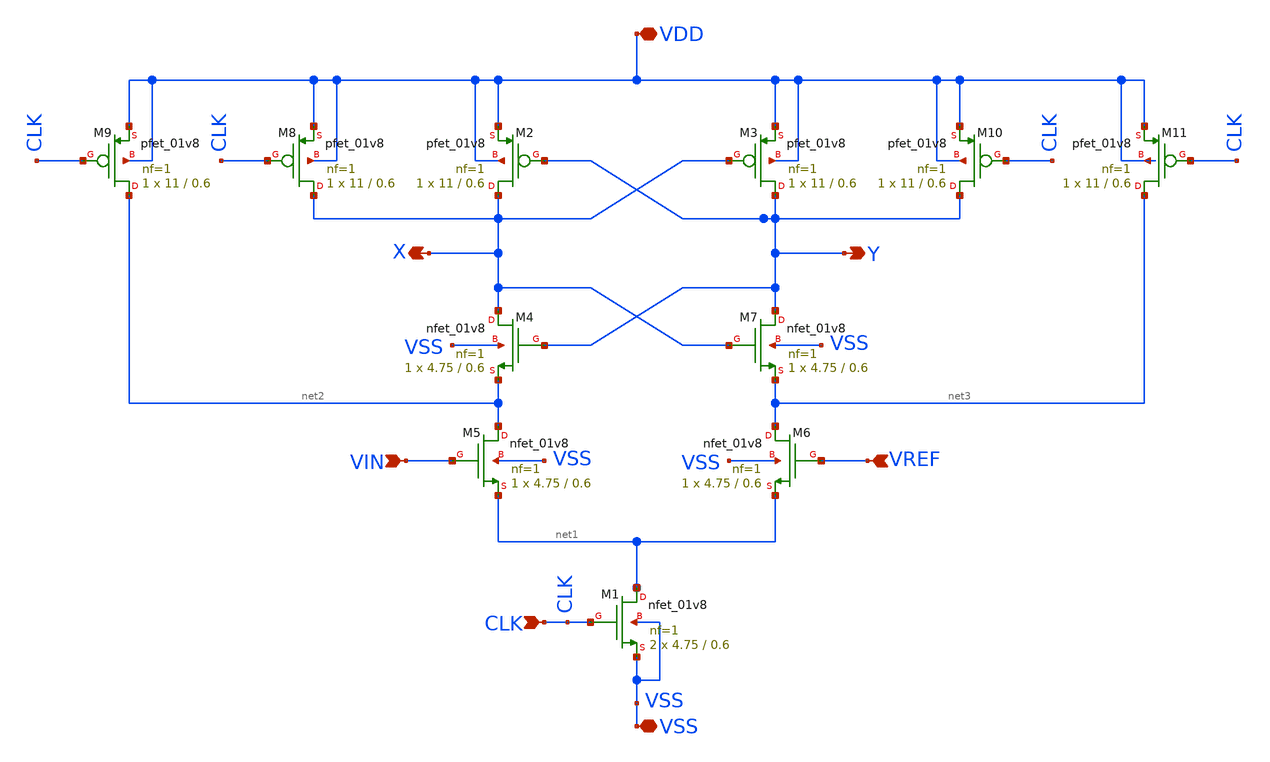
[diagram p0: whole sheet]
** sch_path: strongARM/strongARM_v1_sym.sch
**.subckt strongARM_v1_sym VDD VIN VREF Y X VSS CLK
*.iopin VDD
*.ipin VIN
*.ipin VREF
*.opin Y
*.opin X
*.iopin VSS
*.ipin CLK
XM1 net1 CLK VSS VSS sky130_fd_pr__nfet_01v8 L=0.6 W=4.75 nf=1 ad='int((nf+1)/2) * W/nf * 0.29' as='int((nf+2)/2) * W/nf * 0.29'
+ pd='2*int((nf+1)/2) * (W/nf + 0.29)' ps='2*int((nf+2)/2) * (W/nf + 0.29)' nrd='0.29 / W' nrs='0.29 / W'
+ sa=0 sb=0 sd=0 mult=2 m=2
XM2 X Y VDD VDD sky130_fd_pr__pfet_01v8 L=0.6 W=11 nf=1 ad='int((nf+1)/2) * W/nf * 0.29' as='int((nf+2)/2) * W/nf * 0.29'
+ pd='2*int((nf+1)/2) * (W/nf + 0.29)' ps='2*int((nf+2)/2) * (W/nf + 0.29)' nrd='0.29 / W' nrs='0.29 / W'
+ sa=0 sb=0 sd=0 mult=1 m=1
XM3 Y X VDD VDD sky130_fd_pr__pfet_01v8 L=0.6 W=11 nf=1 ad='int((nf+1)/2) * W/nf * 0.29' as='int((nf+2)/2) * W/nf * 0.29'
+ pd='2*int((nf+1)/2) * (W/nf + 0.29)' ps='2*int((nf+2)/2) * (W/nf + 0.29)' nrd='0.29 / W' nrs='0.29 / W'
+ sa=0 sb=0 sd=0 mult=1 m=1
XM5 net2 VIN net1 VSS sky130_fd_pr__nfet_01v8 L=0.6 W=4.75 nf=1 ad='int((nf+1)/2) * W/nf * 0.29' as='int((nf+2)/2) * W/nf * 0.29'
+ pd='2*int((nf+1)/2) * (W/nf + 0.29)' ps='2*int((nf+2)/2) * (W/nf + 0.29)' nrd='0.29 / W' nrs='0.29 / W'
+ sa=0 sb=0 sd=0 mult=1 m=1
XM4 X Y net2 VSS sky130_fd_pr__nfet_01v8 L=0.6 W=4.75 nf=1 ad='int((nf+1)/2) * W/nf * 0.29' as='int((nf+2)/2) * W/nf * 0.29'
+ pd='2*int((nf+1)/2) * (W/nf + 0.29)' ps='2*int((nf+2)/2) * (W/nf + 0.29)' nrd='0.29 / W' nrs='0.29 / W'
+ sa=0 sb=0 sd=0 mult=1 m=1
XM6 net3 VREF net1 VSS sky130_fd_pr__nfet_01v8 L=0.6 W=4.75 nf=1 ad='int((nf+1)/2) * W/nf * 0.29' as='int((nf+2)/2) * W/nf * 0.29'
+ pd='2*int((nf+1)/2) * (W/nf + 0.29)' ps='2*int((nf+2)/2) * (W/nf + 0.29)' nrd='0.29 / W' nrs='0.29 / W'
+ sa=0 sb=0 sd=0 mult=1 m=1
XM7 Y X net3 VSS sky130_fd_pr__nfet_01v8 L=0.6 W=4.75 nf=1 ad='int((nf+1)/2) * W/nf * 0.29' as='int((nf+2)/2) * W/nf * 0.29'
+ pd='2*int((nf+1)/2) * (W/nf + 0.29)' ps='2*int((nf+2)/2) * (W/nf + 0.29)' nrd='0.29 / W' nrs='0.29 / W'
+ sa=0 sb=0 sd=0 mult=1 m=1
XM8 X CLK VDD VDD sky130_fd_pr__pfet_01v8 L=0.6 W=11 nf=1 ad='int((nf+1)/2) * W/nf * 0.29' as='int((nf+2)/2) * W/nf * 0.29'
+ pd='2*int((nf+1)/2) * (W/nf + 0.29)' ps='2*int((nf+2)/2) * (W/nf + 0.29)' nrd='0.29 / W' nrs='0.29 / W'
+ sa=0 sb=0 sd=0 mult=1 m=1
XM9 net2 CLK VDD VDD sky130_fd_pr__pfet_01v8 L=0.6 W=11 nf=1 ad='int((nf+1)/2) * W/nf * 0.29' as='int((nf+2)/2) * W/nf * 0.29'
+ pd='2*int((nf+1)/2) * (W/nf + 0.29)' ps='2*int((nf+2)/2) * (W/nf + 0.29)' nrd='0.29 / W' nrs='0.29 / W'
+ sa=0 sb=0 sd=0 mult=1 m=1
XM10 Y CLK VDD VDD sky130_fd_pr__pfet_01v8 L=0.6 W=11 nf=1 ad='int((nf+1)/2) * W/nf * 0.29' as='int((nf+2)/2) * W/nf * 0.29'
+ pd='2*int((nf+1)/2) * (W/nf + 0.29)' ps='2*int((nf+2)/2) * (W/nf + 0.29)' nrd='0.29 / W' nrs='0.29 / W'
+ sa=0 sb=0 sd=0 mult=1 m=1
XM11 net3 CLK VDD VDD sky130_fd_pr__pfet_01v8 L=0.6 W=11 nf=1 ad='int((nf+1)/2) * W/nf * 0.29' as='int((nf+2)/2) * W/nf * 0.29'
+ pd='2*int((nf+1)/2) * (W/nf + 0.29)' ps='2*int((nf+2)/2) * (W/nf + 0.29)' nrd='0.29 / W' nrs='0.29 / W'
+ sa=0 sb=0 sd=0 mult=1 m=1
**.ends
.end
